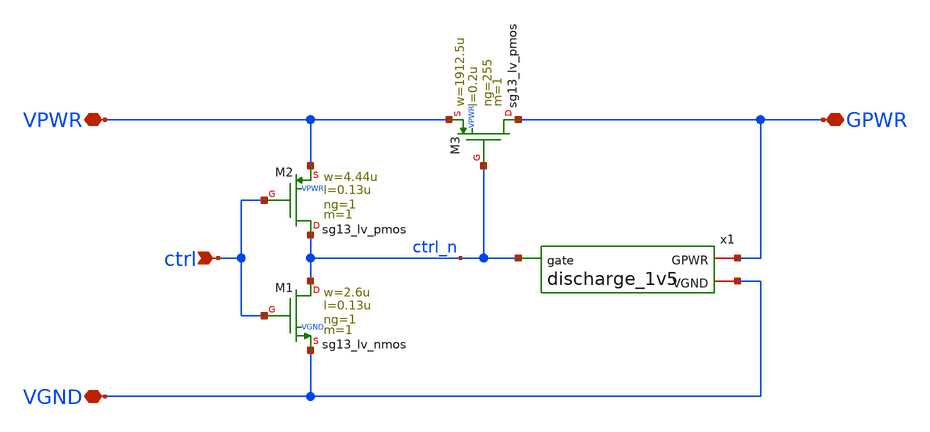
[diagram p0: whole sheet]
** sch_path: pg/ihp-sg13cmos5l/tt_pg_1v5_ll_1/xschem/tt_pg_1v5_ll_1.sch
**.subckt tt_pg_1v5_ll_1 ctrl VPWR VGND GPWR
*.ipin ctrl
*.iopin VPWR
*.iopin VGND
*.iopin GPWR
XM1 ctrl_n ctrl VGND VGND sg13_lv_nmos w=2.6u l=0.13u ng=1 m=1
XM2 ctrl_n ctrl VPWR VPWR sg13_lv_pmos w=4.44u l=0.13u ng=1 m=1
XM3 GPWR ctrl_n VPWR VPWR sg13_lv_pmos w=1912.5u l=0.2u ng=255 m=1
x1 VGND GPWR ctrl_n discharge_1v5
**.ends

* expanding   symbol:  discharge_1v5.sym # of pins=3
** sym_path: pg/ihp-sg13cmos5l/common/xschem/discharge_1v5.sym
** sch_path: pg/ihp-sg13cmos5l/common/xschem/discharge_1v5.sch
.subckt discharge_1v5 VGND GPWR gate
*.iopin GPWR
*.iopin VGND
*.ipin gate
XM1 GPWR gate net3 VGND sg13_lv_nmos w=0.50u l=0.65u ng=1 m=1
XM2 net3 gate net2 VGND sg13_lv_nmos w=0.50u l=0.65u ng=1 m=1
XM3 net2 gate net1 VGND sg13_lv_nmos w=0.50u l=0.65u ng=1 m=1
XM4 net1 gate VGND VGND sg13_lv_nmos w=0.50u l=0.65u ng=1 m=1
XM5 GPWR gate net6 VGND sg13_lv_nmos w=0.50u l=0.65u ng=1 m=1
XM6 net6 gate net5 VGND sg13_lv_nmos w=0.50u l=0.65u ng=1 m=1
XM7 net5 gate net4 VGND sg13_lv_nmos w=0.50u l=0.65u ng=1 m=1
XM8 net4 gate VGND VGND sg13_lv_nmos w=0.50u l=0.65u ng=1 m=1
.ends

.end
